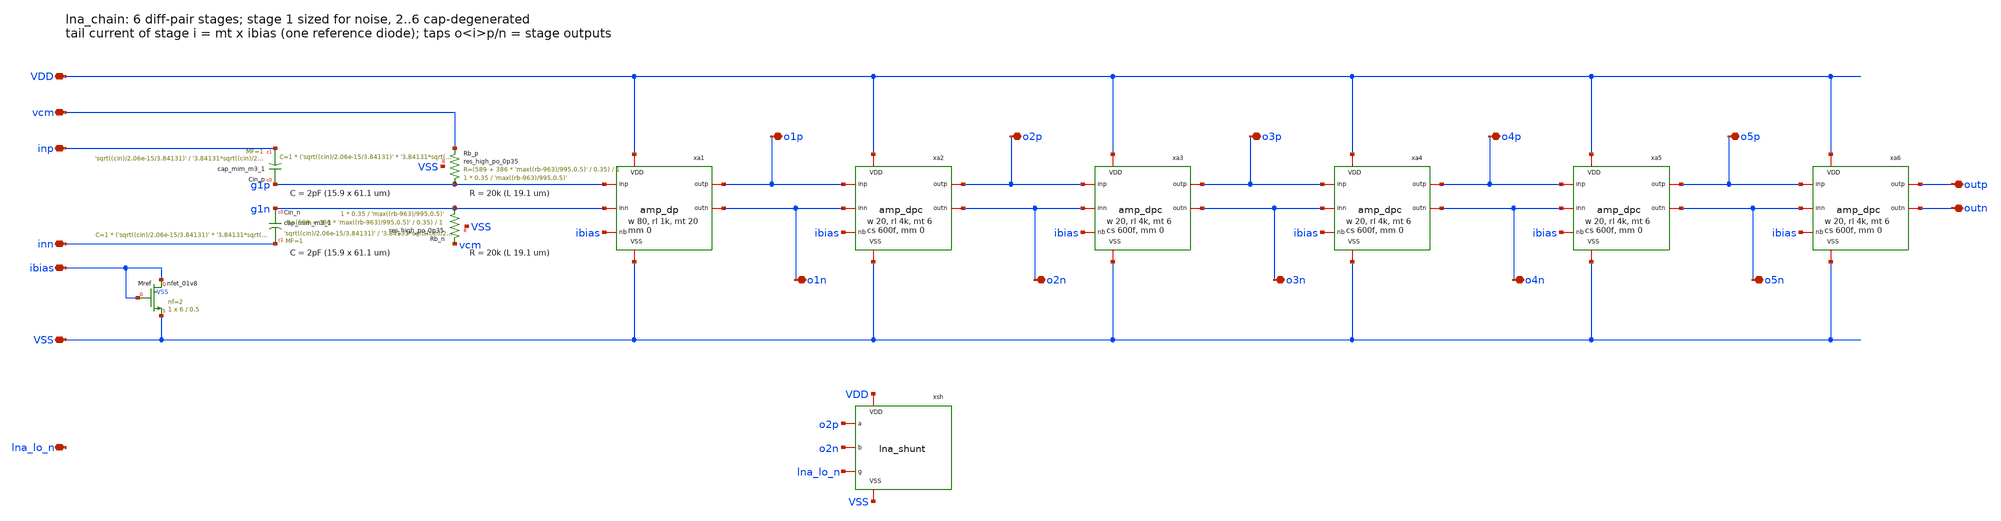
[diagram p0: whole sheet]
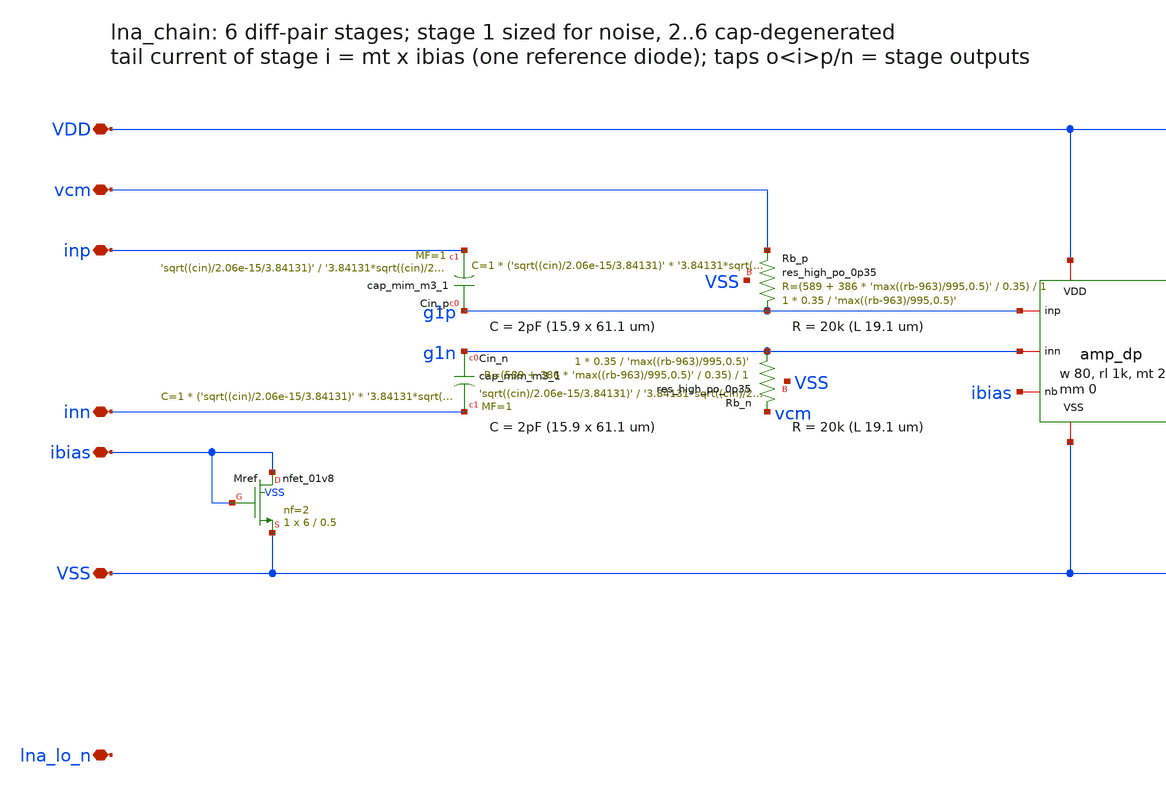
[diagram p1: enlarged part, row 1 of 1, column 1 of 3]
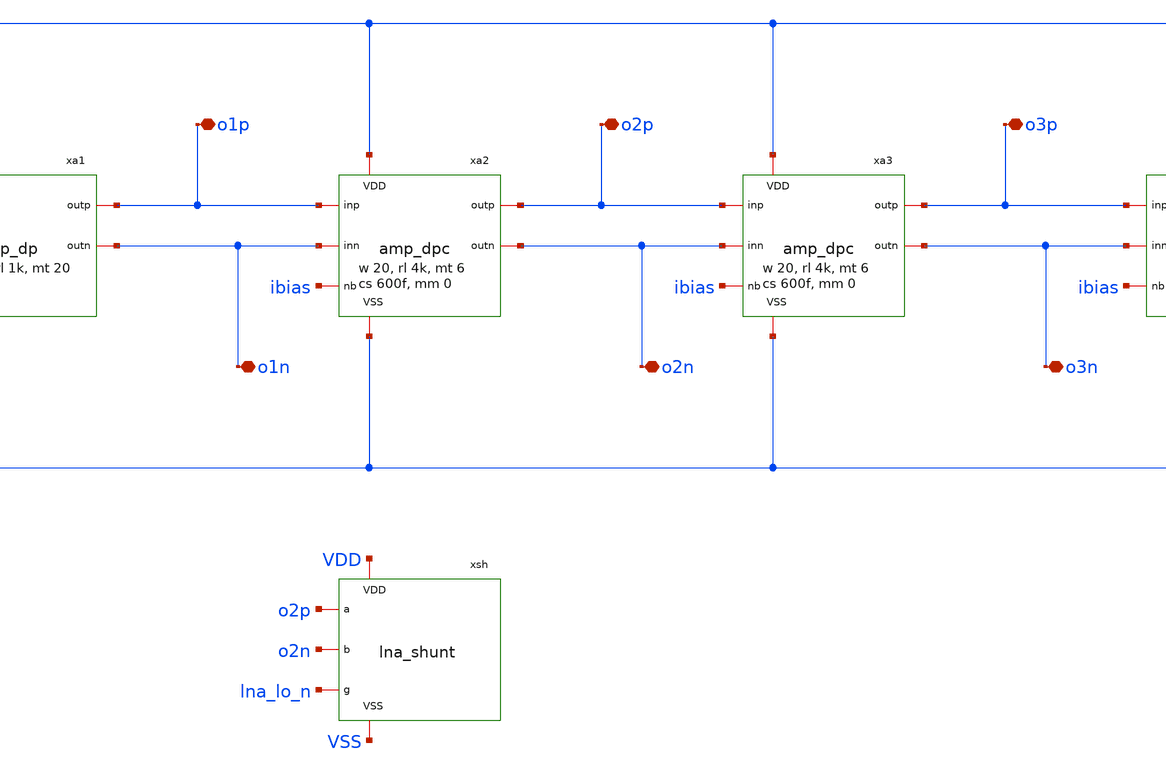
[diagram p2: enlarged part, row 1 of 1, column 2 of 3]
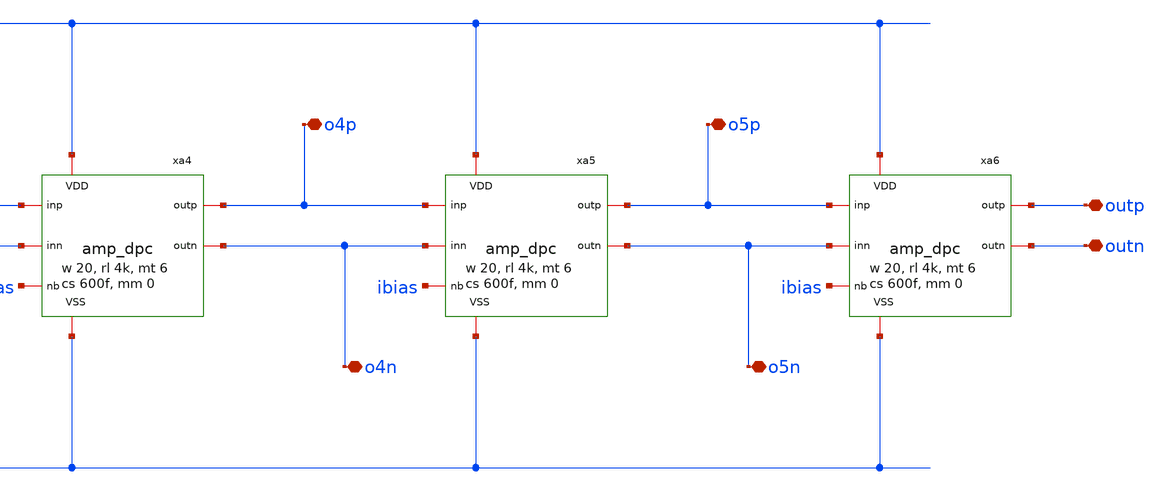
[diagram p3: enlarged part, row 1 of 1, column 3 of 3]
** sch_path: xschem/lna_chain.sch
**.subckt lna_chain VDD VSS ibias vcm lna_lo_n inp inn outp outn o1p o1n o2p o2n o3p o3n o4p o4n o5p
*+ o5n
*.iopin VDD
*.iopin VSS
*.iopin ibias
*.iopin vcm
*.iopin lna_lo_n
*.iopin inp
*.iopin inn
*.iopin outp
*.iopin outn
*.iopin o1p
*.iopin o1n
*.iopin o2p
*.iopin o2n
*.iopin o3p
*.iopin o3n
*.iopin o4p
*.iopin o4n
*.iopin o5p
*.iopin o5n
XMref ibias ibias VSS VSS sky130_fd_pr__nfet_01v8 L=0.5 W=6 nf=2 ad='int((nf+1)/2) * W/nf * 0.29' as='int((nf+2)/2) * W/nf * 0.29'
+ pd='2*int((nf+1)/2) * (W/nf + 0.29)' ps='2*int((nf+2)/2) * (W/nf + 0.29)' nrd='0.29 / W' nrs='0.29 / W'
+ sa=0 sb=0 sd=0 mult=1 m=1
XCin_p g1p inp sky130_fd_pr__cap_mim_m3_1 W='sqrt((cin)/2.06e-15/3.84131)' L='3.84131*sqrt((cin)/2.06e-15/3.84131)'
+ MF=1 m=1
XRb_p g1p vcm VSS sky130_fd_pr__res_high_po_0p35 L='max((rb-963)/995,0.5)' mult=1 m=1
XCin_n g1n inn sky130_fd_pr__cap_mim_m3_1 W='sqrt((cin)/2.06e-15/3.84131)' L='3.84131*sqrt((cin)/2.06e-15/3.84131)'
+ MF=1 m=1
XRb_n g1n vcm VSS sky130_fd_pr__res_high_po_0p35 L='max((rb-963)/995,0.5)' mult=1 m=1
xa1 g1p g1n ibias o1p o1n VDD VSS amp_dp w='w1' l=0.15 rl='rl1' wt=6 mt='mt1' mm='mm'
xa2 o1p o1n ibias o2p o2n VDD VSS amp_dpc w='w2' l=0.15 rl='rl2' wt=6 mt='mt2' cs='cs'
xa3 o2p o2n ibias o3p o3n VDD VSS amp_dpc w='w2' l=0.15 rl='rl2' wt=6 mt='mt2' cs='cs'
xa4 o3p o3n ibias o4p o4n VDD VSS amp_dpc w='w2' l=0.15 rl='rl2' wt=6 mt='mt2' cs='cs'
xa5 o4p o4n ibias o5p o5n VDD VSS amp_dpc w='w2' l=0.15 rl='rl2' wt=6 mt='mt2' cs='cs'
xa6 o5p o5n ibias outp outn VDD VSS amp_dpc w='w2' l=0.15 rl='rl2' wt=6 mt='mt2' cs='cs'
xsh o2p o2n lna_lo_n VDD VSS lna_shunt rh=393 wsw=15 rg=20k
**.ends

* expanding   symbol:  amp_dp.sym # of pins=7
** sym_path: xschem/amp_dp.sym
** sch_path: xschem/amp_dp.sch
.subckt amp_dp inp inn nb outp outn VDD VSS  w=80 l=0.15 rl=1k wt=6 mt=20 mm=0
*.iopin VDD
*.iopin VSS
*.iopin nb
*.iopin inp
*.iopin inn
*.iopin outp
*.iopin outn
XRl_p outn VDD VSS sky130_fd_pr__res_high_po_1p41 L='max((rl-278)/230.3,0.5)' mult=1 m=1
XMp outn inp tail VSS sky130_fd_pr__nfet_01v8 L='l' W='w*(1+mm/2)' nf=4 ad='int((nf+1)/2) * W/nf * 0.29'
+ as='int((nf+2)/2) * W/nf * 0.29' pd='2*int((nf+1)/2) * (W/nf + 0.29)' ps='2*int((nf+2)/2) * (W/nf + 0.29)'
+ nrd='0.29 / W' nrs='0.29 / W' sa=0 sb=0 sd=0 mult=1 m=1
XRl_n outp VDD VSS sky130_fd_pr__res_high_po_1p41 L='max((rl-278)/230.3,0.5)' mult=1 m=1
XMn outp inn tail VSS sky130_fd_pr__nfet_01v8 L='l' W='w*(1-mm/2)' nf=4 ad='int((nf+1)/2) * W/nf * 0.29'
+ as='int((nf+2)/2) * W/nf * 0.29' pd='2*int((nf+1)/2) * (W/nf + 0.29)' ps='2*int((nf+2)/2) * (W/nf + 0.29)'
+ nrd='0.29 / W' nrs='0.29 / W' sa=0 sb=0 sd=0 mult=1 m=1
XMtail tail nb VSS VSS sky130_fd_pr__nfet_01v8 L=0.5 W='wt' nf=2 ad='int((nf+1)/2) * W/nf * 0.29' as='int((nf+2)/2) * W/nf * 0.29'
+ pd='2*int((nf+1)/2) * (W/nf + 0.29)' ps='2*int((nf+2)/2) * (W/nf + 0.29)' nrd='0.29 / W' nrs='0.29 / W'
+ sa=0 sb=0 sd=0 mult='mt' m='mt'
.ends


* expanding   symbol:  amp_dpc.sym # of pins=7
** sym_path: xschem/amp_dpc.sym
** sch_path: xschem/amp_dpc.sch
.subckt amp_dpc inp inn nb outp outn VDD VSS  w=20 l=0.15 rl=4k wt=6 mt=6 cs=0.6p
*.iopin VDD
*.iopin VSS
*.iopin nb
*.iopin inp
*.iopin inn
*.iopin outp
*.iopin outn
XRl_p outn VDD VSS sky130_fd_pr__res_high_po_0p69 L='max((rl-526)/470.9,0.5)' mult=1 m=1
XMp outn inp sp VSS sky130_fd_pr__nfet_01v8 L='l' W='w*(1+mm/2)' nf=4 ad='int((nf+1)/2) * W/nf * 0.29'
+ as='int((nf+2)/2) * W/nf * 0.29' pd='2*int((nf+1)/2) * (W/nf + 0.29)' ps='2*int((nf+2)/2) * (W/nf + 0.29)'
+ nrd='0.29 / W' nrs='0.29 / W' sa=0 sb=0 sd=0 mult=1 m=1
XMtail_p sp nb VSS VSS sky130_fd_pr__nfet_01v8 L=0.5 W='wt' nf=2 ad='int((nf+1)/2) * W/nf * 0.29' as='int((nf+2)/2) * W/nf * 0.29'
+ pd='2*int((nf+1)/2) * (W/nf + 0.29)' ps='2*int((nf+2)/2) * (W/nf + 0.29)' nrd='0.29 / W' nrs='0.29 / W'
+ sa=0 sb=0 sd=0 mult='mt/2' m='mt/2'
XRl_n outp VDD VSS sky130_fd_pr__res_high_po_0p69 L='max((rl-526)/470.9,0.5)' mult=1 m=1
XMn outp inn sn VSS sky130_fd_pr__nfet_01v8 L='l' W='w*(1-mm/2)' nf=4 ad='int((nf+1)/2) * W/nf * 0.29'
+ as='int((nf+2)/2) * W/nf * 0.29' pd='2*int((nf+1)/2) * (W/nf + 0.29)' ps='2*int((nf+2)/2) * (W/nf + 0.29)'
+ nrd='0.29 / W' nrs='0.29 / W' sa=0 sb=0 sd=0 mult=1 m=1
XMtail_n sn nb VSS VSS sky130_fd_pr__nfet_01v8 L=0.5 W='wt' nf=2 ad='int((nf+1)/2) * W/nf * 0.29' as='int((nf+2)/2) * W/nf * 0.29'
+ pd='2*int((nf+1)/2) * (W/nf + 0.29)' ps='2*int((nf+2)/2) * (W/nf + 0.29)' nrd='0.29 / W' nrs='0.29 / W'
+ sa=0 sb=0 sd=0 mult='mt/2' m='mt/2'
XCs_a sn sp sky130_fd_pr__cap_mim_m3_1 W='sqrt((cs/2)/2.06e-15/3.13676)' L='3.13676*sqrt((cs/2)/2.06e-15/3.13676)'
+ MF=1 m=1
XCs_b sp sn sky130_fd_pr__cap_mim_m3_1 W='sqrt((cs/2)/2.06e-15/3.13676)' L='3.13676*sqrt((cs/2)/2.06e-15/3.13676)'
+ MF=1 m=1
.ends


* expanding   symbol:  lna_shunt.sym # of pins=5
** sym_path: xschem/lna_shunt.sym
** sch_path: xschem/lna_shunt.sch
.subckt lna_shunt a b g VDD VSS  rh=393 wsw=15 rg=20k
*.iopin VDD
*.iopin VSS
*.iopin a
*.iopin b
*.iopin g
XRh_a sa a VSS sky130_fd_pr__res_high_po_1p41 L='max((rh-278)/230.3,0.5)' mult=1 m=1
XRh_b b sb VSS sky130_fd_pr__res_high_po_1p41 L='max((rh-278)/230.3,0.5)' mult=1 m=1
XMsw sb gi sa VDD sky130_fd_pr__pfet_01v8 L=0.15 W='wsw' nf=6 ad='int((nf+1)/2) * W/nf * 0.29' as='int((nf+2)/2) * W/nf * 0.29'
+ pd='2*int((nf+1)/2) * (W/nf + 0.29)' ps='2*int((nf+2)/2) * (W/nf + 0.29)' nrd='0.29 / W' nrs='0.29 / W'
+ sa=0 sb=0 sd=0 mult=1 m=1
XRg g gi VSS sky130_fd_pr__res_xhigh_po_0p35 L='max((rg-0)/7379,0.5)' mult=1 m=1
XMcap VDD gi VDD VDD sky130_fd_pr__pfet_01v8 L=5 W=5 nf=1 ad='int((nf+1)/2) * W/nf * 0.29' as='int((nf+2)/2) * W/nf * 0.29'
+ pd='2*int((nf+1)/2) * (W/nf + 0.29)' ps='2*int((nf+2)/2) * (W/nf + 0.29)' nrd='0.29 / W' nrs='0.29 / W'
+ sa=0 sb=0 sd=0 mult=1 m=1
.ends

.end
